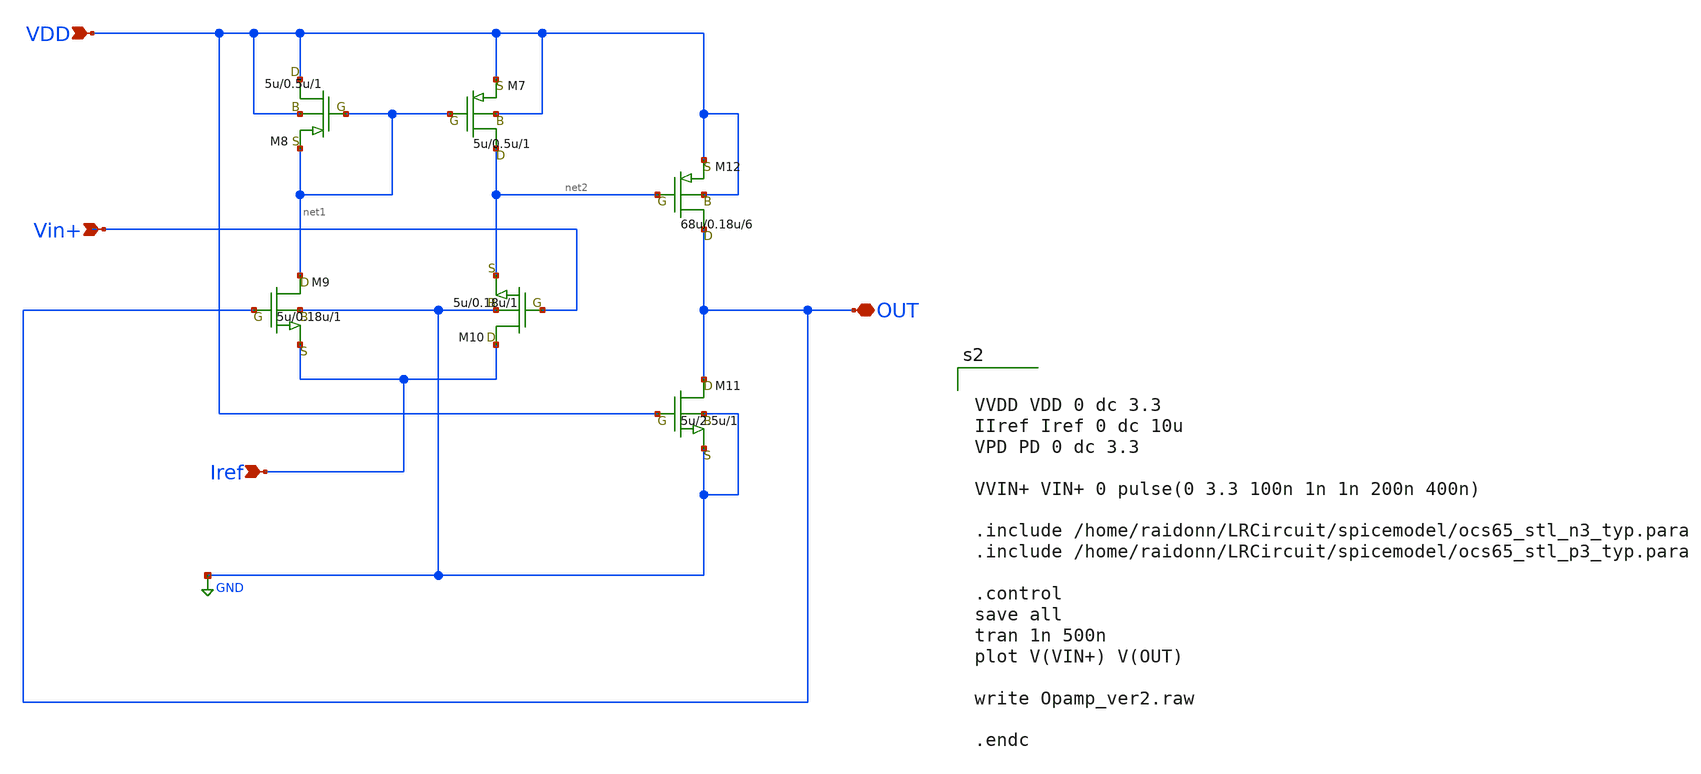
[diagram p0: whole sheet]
** sch_path: LR_Work3/Opamp_ver2.sch
**.subckt Opamp_ver2 VDD Vin+ OUT Iref
*.ipin VDD
*.ipin Vin+
*.iopin OUT
*.ipin Iref
M7 net2 net1 VDD VDD p3.0 w=5u l=0.5u as=0 ps=0 ad=0 pd=0 m=1
M8 VDD net1 net1 VDD p3.0 w=5u l=0.5u as=0 ps=0 ad=0 pd=0 m=1
M9 net1 OUT Iref GND n3.0 w=5u l=0.18u as=0 ps=0 ad=0 pd=0 m=1
M10 Iref Vin+ net2 GND n3.0 w=5u l=0.18u as=0 ps=0 ad=0 pd=0 m=1
M11 OUT VDD GND GND n3.0 w=5u l=2.5u as=0 ps=0 ad=0 pd=0 m=1
M12 OUT net2 VDD VDD p3.0 w=68u l=0.18u as=0 ps=0 ad=0 pd=0 m=6
**** begin user architecture code


VVDD VDD 0 dc 3.3
IIref Iref 0 dc 10u
VPD PD 0 dc 3.3

VVIN+ VIN+ 0 pulse(0 3.3 100n 1n 1n 200n 400n)

.include /home/raidonn/LRCircuit/spicemodel/ocs65_stl_n3_typ.para
.include /home/raidonn/LRCircuit/spicemodel/ocs65_stl_p3_typ.para

.control
save all
tran 1n 500n
plot V(VIN+) V(OUT)

write Opamp_ver2.raw

.endc

**** end user architecture code
**.ends
.GLOBAL GND
.end
